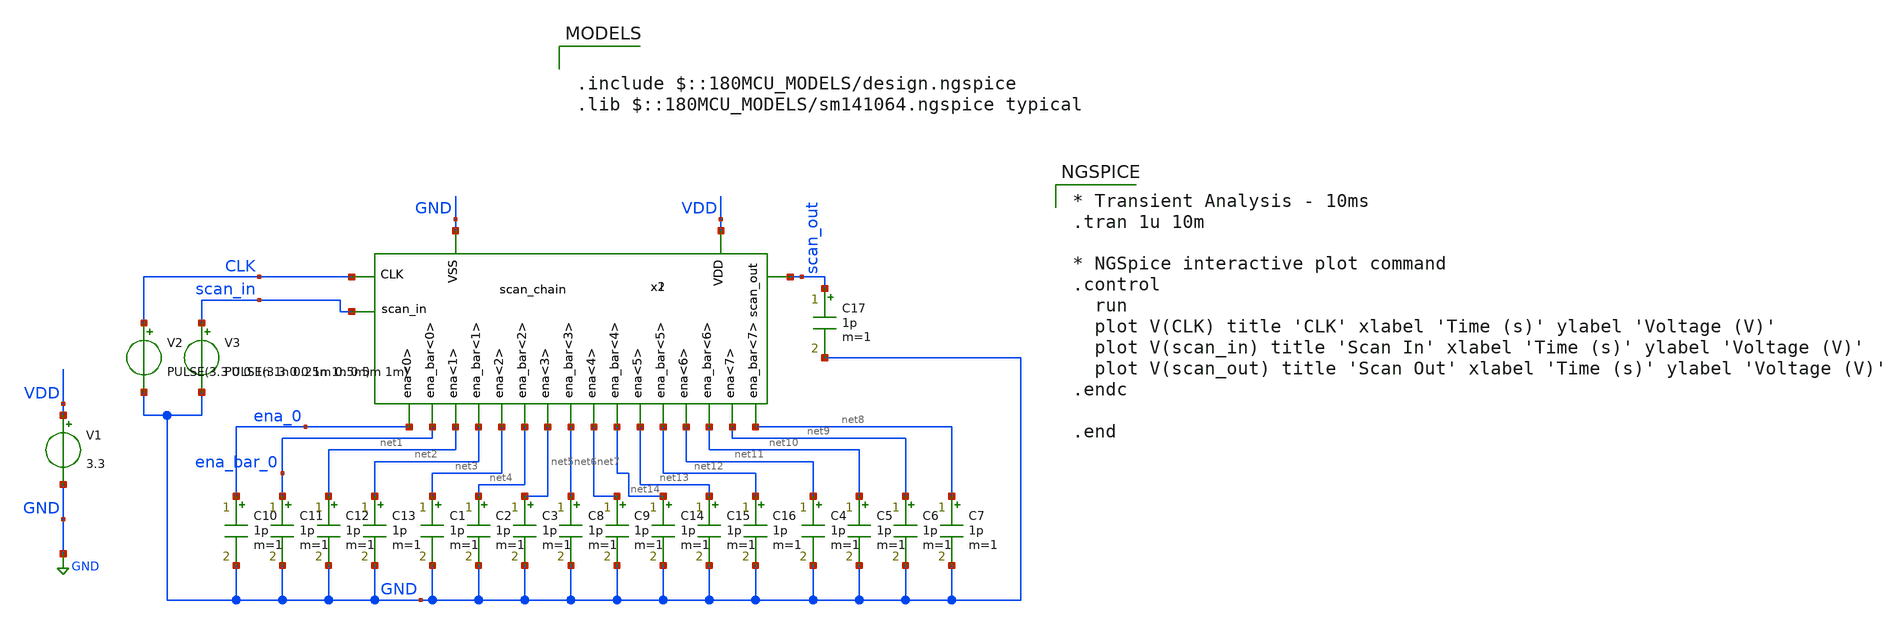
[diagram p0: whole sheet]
** sch_path: designs/libs/core_digital/tb/TB_scan_chain.sch
**.subckt TB_scan_chain
x1 VDD scan_out net13 net7 net11 net9 net3 net1 ena_0 net5 scan_in net2 net8 net4 net10 net12 net14
+ net6 ena_bar_0 CLK GND scan_chain
V1 VDD GND 3.3
C1 net3 GND 1p m=1
C2 net4 GND 1p m=1
C3 net5 GND 1p m=1
C8 net6 GND 1p m=1
C10 ena_0 GND 1p m=1
C11 ena_bar_0 GND 1p m=1
C12 net1 GND 1p m=1
C13 net2 GND 1p m=1
C4 net11 GND 1p m=1
C5 net10 GND 1p m=1
C6 net9 GND 1p m=1
C7 net8 GND 1p m=1
C9 net7 GND 1p m=1
C14 net14 GND 1p m=1
C15 net13 GND 1p m=1
C16 net12 GND 1p m=1
C17 scan_out GND 1p m=1
V2 CLK GND PULSE(3.3 0 0 1n 1n 0.25m 0.5m)
V3 scan_in GND PULSE(3.3 0 0 1n 1n 0.5m 1m)
x2 VDD scan_out net13 net7 net11 net9 net3 net1 ena_0 net5 scan_in net2 net8 net4 net10 net12 net14
+ net6 ena_bar_0 CLK GND scan_chain
**** begin user architecture code

.include $::180MCU_MODELS/design.ngspice
.lib $::180MCU_MODELS/sm141064.ngspice typical

 * Transient Analysis - 10ms
.tran 1u 10m

* NGSpice interactive plot command
.control
  run
  plot V(CLK) title 'CLK' xlabel 'Time (s)' ylabel 'Voltage (V)'
  plot V(scan_in) title 'Scan In' xlabel 'Time (s)' ylabel 'Voltage (V)'
  plot V(scan_out) title 'Scan Out' xlabel 'Time (s)' ylabel 'Voltage (V)'
.endc

.end
**** end user architecture code
**.ends
.GLOBAL GND
.end
